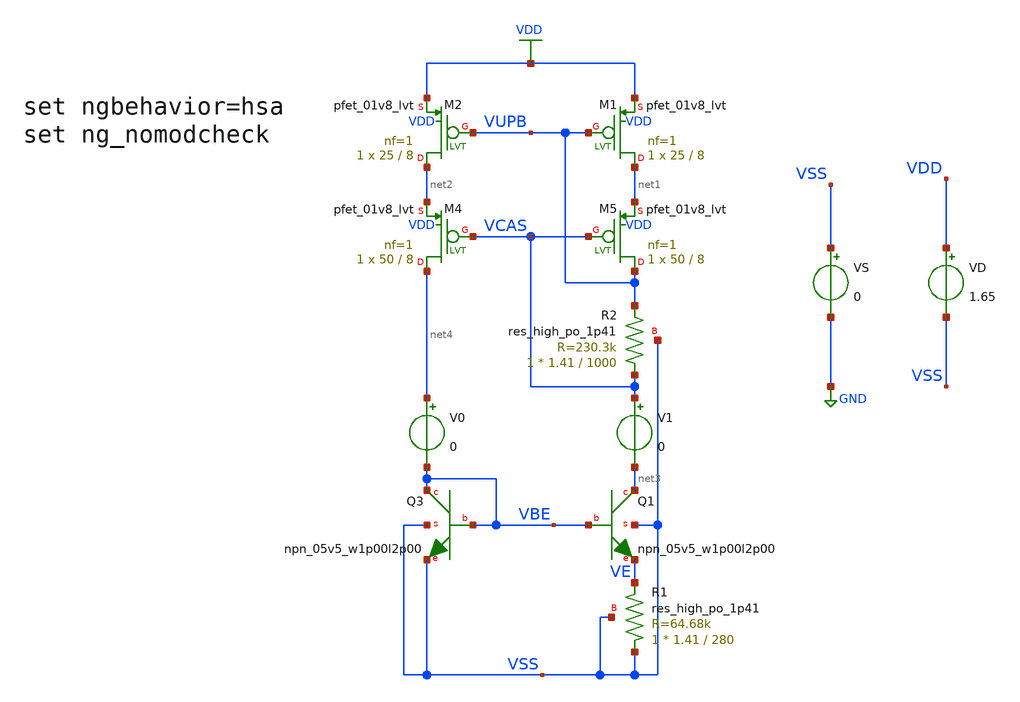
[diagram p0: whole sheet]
** sch_path: testbenches/temp_char_ptat_ctat.sch
**.subckt temp_char_ptat_ctat
VD VDD VSS 1.65
.save i(vd)
VS VSS GND 0
XM1 net1 VUPB VDD VDD sky130_fd_pr__pfet_01v8_lvt L=8 W=25 nf=1 ad='int((nf+1)/2) * W/nf * 0.29' as='int((nf+2)/2) * W/nf * 0.29'
+ pd='2*int((nf+1)/2) * (W/nf + 0.29)' ps='2*int((nf+2)/2) * (W/nf + 0.29)' nrd='0.29 / W' nrs='0.29 / W'
+ sa=0 sb=0 sd=0 mult=1 m=1
XM2 net2 VUPB VDD VDD sky130_fd_pr__pfet_01v8_lvt L=8 W=25 nf=1 ad='int((nf+1)/2) * W/nf * 0.29' as='int((nf+2)/2) * W/nf * 0.29'
+ pd='2*int((nf+1)/2) * (W/nf + 0.29)' ps='2*int((nf+2)/2) * (W/nf + 0.29)' nrd='0.29 / W' nrs='0.29 / W'
+ sa=0 sb=0 sd=0 mult=1 m=1
XQ1 net3 VBE VE VSS sky130_fd_pr__npn_05v5_w1p00l2p00
XQ3 VBE VBE VSS VSS sky130_fd_pr__npn_05v5_w1p00l2p00
V0 net4 VBE 0
.save i(v0)
XR1 VSS VE VSS sky130_fd_pr__res_high_po_1p41 L=280 mult=1 m=1
XM4 net4 VCAS net2 VDD sky130_fd_pr__pfet_01v8_lvt L=8 W=50 nf=1 ad='int((nf+1)/2) * W/nf * 0.29' as='int((nf+2)/2) * W/nf * 0.29'
+ pd='2*int((nf+1)/2) * (W/nf + 0.29)' ps='2*int((nf+2)/2) * (W/nf + 0.29)' nrd='0.29 / W' nrs='0.29 / W'
+ sa=0 sb=0 sd=0 mult=1 m=1
XM5 VUPB VCAS net1 VDD sky130_fd_pr__pfet_01v8_lvt L=8 W=50 nf=1 ad='int((nf+1)/2) * W/nf * 0.29' as='int((nf+2)/2) * W/nf * 0.29'
+ pd='2*int((nf+1)/2) * (W/nf + 0.29)' ps='2*int((nf+2)/2) * (W/nf + 0.29)' nrd='0.29 / W' nrs='0.29 / W'
+ sa=0 sb=0 sd=0 mult=1 m=1
XR2 VCAS VUPB VSS sky130_fd_pr__res_high_po_1p41 L=1000 mult=1 m=1
V1 VCAS net3 0
.save i(v1)
**** begin user architecture code


** Analysis Requests **
** Outputs Requests **
.option wnflag=1
.option savecurrents
.control
save all
dc temp -40 125 5 VD 1.65 3.3 0.825
remzerovec
wrdata ~/.xschem/simulations/temp_char_ptat_ctat.txt i(V0) i(V1)/i(V0) v(VBE) v(VUPB)
*plot V(VBE), V(VUPB)
plot V(VUPB)
plot I(V1)/I(V0)
plot I(V0), I(V1)
.endc



** opencircuitdesign pdks install
.lib /foss/pdks/sky130A/libs.tech/ngspice/sky130.lib.corners.spice ssll

**** end user architecture code
**.ends
.GLOBAL GND
.GLOBAL VDD
.end
